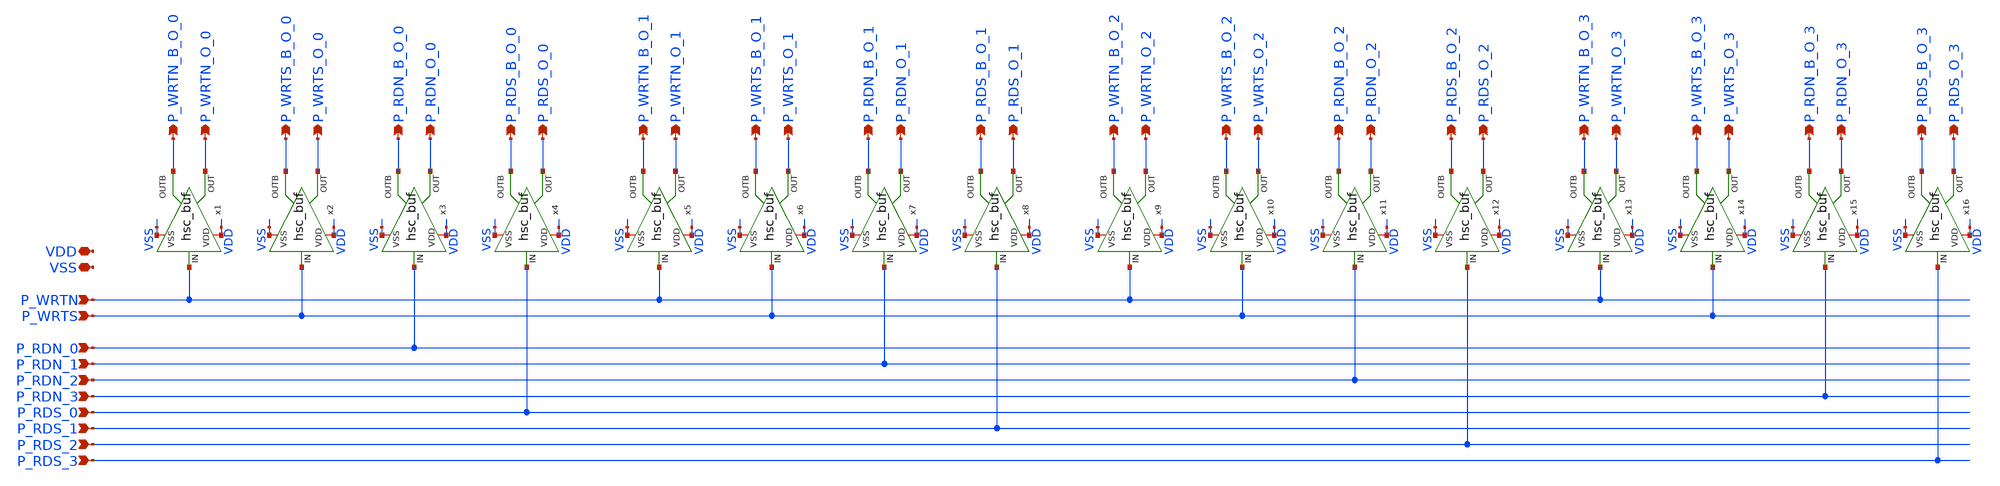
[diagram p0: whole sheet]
** sch_path: member_project/imager/YuMaehashi/design/hsc.sch
**.subckt hsc VDD VSS P_RDS_3 P_RDN_3 P_RDS_2 P_RDN_2 P_RDS_1 P_RDN_1 P_RDS_0 P_RDN_0 P_WRTS P_WRTN
*+ P_WRTN_O_0 P_WRTN_B_O_0 P_WRTS_O_0 P_WRTS_B_O_0 P_RDN_B_O_0 P_RDN_O_0 P_RDS_B_O_0 P_RDS_O_0 P_WRTN_O_1
*+ P_WRTN_B_O_1 P_WRTS_O_1 P_WRTS_B_O_1 P_RDN_B_O_1 P_RDN_O_1 P_RDS_B_O_1 P_RDS_O_1 P_WRTN_O_2 P_WRTN_B_O_2
*+ P_WRTS_O_2 P_WRTS_B_O_2 P_RDN_B_O_2 P_RDN_O_2 P_RDS_B_O_2 P_RDS_O_2 P_WRTN_O_3 P_WRTN_B_O_3 P_WRTS_O_3
*+ P_WRTS_B_O_3 P_RDN_B_O_3 P_RDN_O_3 P_RDS_B_O_3 P_RDS_O_3
*.iopin VDD
*.iopin VSS
*.ipin P_RDS_3
*.ipin P_RDN_3
*.ipin P_RDS_2
*.ipin P_RDN_2
*.ipin P_RDS_1
*.ipin P_RDN_1
*.ipin P_RDS_0
*.ipin P_RDN_0
*.ipin P_WRTS
*.ipin P_WRTN
*.opin P_WRTN_O_0
*.opin P_WRTN_B_O_0
*.opin P_WRTS_O_0
*.opin P_WRTS_B_O_0
*.opin P_RDN_B_O_0
*.opin P_RDN_O_0
*.opin P_RDS_B_O_0
*.opin P_RDS_O_0
*.opin P_WRTN_O_1
*.opin P_WRTN_B_O_1
*.opin P_WRTS_O_1
*.opin P_WRTS_B_O_1
*.opin P_RDN_B_O_1
*.opin P_RDN_O_1
*.opin P_RDS_B_O_1
*.opin P_RDS_O_1
*.opin P_WRTN_O_2
*.opin P_WRTN_B_O_2
*.opin P_WRTS_O_2
*.opin P_WRTS_B_O_2
*.opin P_RDN_B_O_2
*.opin P_RDN_O_2
*.opin P_RDS_B_O_2
*.opin P_RDS_O_2
*.opin P_WRTN_O_3
*.opin P_WRTN_B_O_3
*.opin P_WRTS_O_3
*.opin P_WRTS_B_O_3
*.opin P_RDN_B_O_3
*.opin P_RDN_O_3
*.opin P_RDS_B_O_3
*.opin P_RDS_O_3
x1 VDD P_WRTN P_WRTN_O_0 VSS P_WRTN_B_O_0 hsc_buf
x2 VDD P_WRTS P_WRTS_O_0 VSS P_WRTS_B_O_0 hsc_buf
x3 VDD P_RDN_0 P_RDN_O_0 VSS P_RDN_B_O_0 hsc_buf
x4 VDD P_RDS_0 P_RDS_O_0 VSS P_RDS_B_O_0 hsc_buf
x5 VDD P_WRTN P_WRTN_O_1 VSS P_WRTN_B_O_1 hsc_buf
x6 VDD P_WRTS P_WRTS_O_1 VSS P_WRTS_B_O_1 hsc_buf
x7 VDD P_RDN_1 P_RDN_O_1 VSS P_RDN_B_O_1 hsc_buf
x8 VDD P_RDS_1 P_RDS_O_1 VSS P_RDS_B_O_1 hsc_buf
x9 VDD P_WRTN P_WRTN_O_2 VSS P_WRTN_B_O_2 hsc_buf
x10 VDD P_WRTS P_WRTS_O_2 VSS P_WRTS_B_O_2 hsc_buf
x11 VDD P_RDN_2 P_RDN_O_2 VSS P_RDN_B_O_2 hsc_buf
x12 VDD P_RDS_2 P_RDS_O_2 VSS P_RDS_B_O_2 hsc_buf
x13 VDD P_WRTN P_WRTN_O_3 VSS P_WRTN_B_O_3 hsc_buf
x14 VDD P_WRTS P_WRTS_O_3 VSS P_WRTS_B_O_3 hsc_buf
x15 VDD P_RDN_3 P_RDN_O_3 VSS P_RDN_B_O_3 hsc_buf
x16 VDD P_RDS_3 P_RDS_O_3 VSS P_RDS_B_O_3 hsc_buf
**.ends

* expanding   symbol:  2026_imager/hsc_buf.sym # of pins=5
** sym_path: member_project/imager/YuMaehashi/design/hsc_buf.sym
** sch_path: member_project/imager/YuMaehashi/design/hsc_buf.sch
.subckt hsc_buf VDD IN OUT VSS OUTB
*.iopin VSS
*.ipin IN
*.opin OUT
*.iopin VDD
*.opin OUTB
XXM1 net1 IN VSS VSS NMOS w=3.4u l=1u nrd=0 nrs=0 m=1
XXM2 net1 IN VDD VDD PMOS w=10.2u l=1u nrd=0 nrs=0 m=1
XXM3 OUT net1 VSS VSS NMOS w=3.4u l=1u nrd=0 nrs=0 m=4
XXM4 OUT net1 VDD VDD PMOS w=10.2u l=1u nrd=0 nrs=0 m=4
XXM5 OUTB OUT VSS VSS NMOS w=3.4u l=1u nrd=0 nrs=0 m=4
XXM6 OUTB OUT VDD VDD PMOS w=10.2u l=1u nrd=0 nrs=0 m=4
.ends

.end
